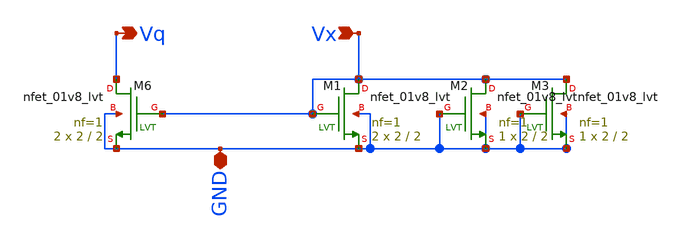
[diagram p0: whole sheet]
** sch_path: lvs/ampcurrentsource.sch
**.subckt ampcurrentsource Vq Vx GND
*.opin Vq
*.ipin Vx
*.iopin GND
XM6 Vq Vx GND GND sky130_fd_pr__nfet_01v8_lvt L=2 W=2 nf=1 ad='int((nf+1)/2) * W/nf * 0.29' as='int((nf+2)/2) * W/nf * 0.29'
+ pd='2*int((nf+1)/2) * (W/nf + 0.29)' ps='2*int((nf+2)/2) * (W/nf + 0.29)' nrd='0.29 / W' nrs='0.29 / W'
+ sa=0 sb=0 sd=0 mult=2 m=2
XM1 Vx Vx GND GND sky130_fd_pr__nfet_01v8_lvt L=2 W=2 nf=1 ad='int((nf+1)/2) * W/nf * 0.29' as='int((nf+2)/2) * W/nf * 0.29'
+ pd='2*int((nf+1)/2) * (W/nf + 0.29)' ps='2*int((nf+2)/2) * (W/nf + 0.29)' nrd='0.29 / W' nrs='0.29 / W'
+ sa=0 sb=0 sd=0 mult=2 m=2
XM2 Vx GND GND GND sky130_fd_pr__nfet_01v8_lvt L=2 W=2 nf=1 ad='int((nf+1)/2) * W/nf * 0.29' as='int((nf+2)/2) * W/nf * 0.29'
+ pd='2*int((nf+1)/2) * (W/nf + 0.29)' ps='2*int((nf+2)/2) * (W/nf + 0.29)' nrd='0.29 / W' nrs='0.29 / W'
+ sa=0 sb=0 sd=0 mult=1 m=1
XM3 Vx GND GND GND sky130_fd_pr__nfet_01v8_lvt L=2 W=2 nf=1 ad='int((nf+1)/2) * W/nf * 0.29' as='int((nf+2)/2) * W/nf * 0.29'
+ pd='2*int((nf+1)/2) * (W/nf + 0.29)' ps='2*int((nf+2)/2) * (W/nf + 0.29)' nrd='0.29 / W' nrs='0.29 / W'
+ sa=0 sb=0 sd=0 mult=1 m=1
**.ends
.end
